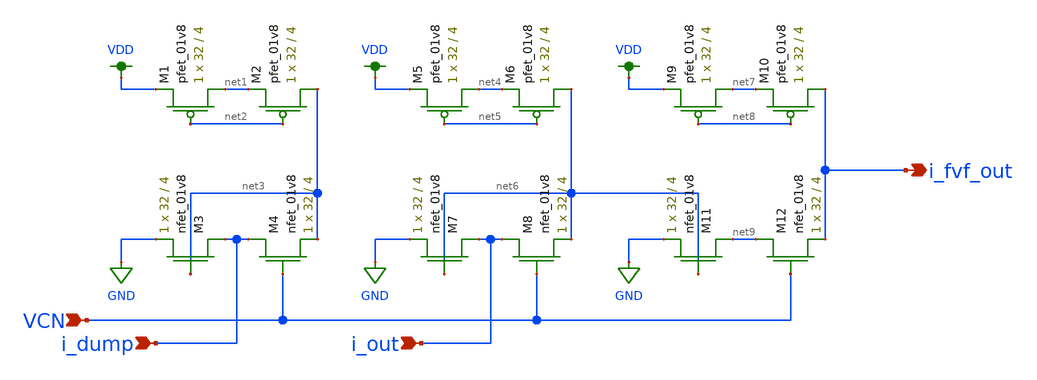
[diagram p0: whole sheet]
** sch_path: schemas/LDS_FVF_BLOCK.sch
**.subckt LDS_FVF_BLOCK i_fvf_out i_dump i_out VCN
*.opin i_fvf_out
*.ipin i_dump
*.ipin i_out
*.ipin VCN
XM1 net1 net2 VDD VDD sky130_fd_pr__pfet_01v8 L=4 W=32 nf=1 ad='int((nf+1)/2) * W/nf * 0.29' as='int((nf+2)/2) * W/nf * 0.29'
+ pd='2*int((nf+1)/2) * (W/nf + 0.29)' ps='2*int((nf+2)/2) * (W/nf + 0.29)' nrd='0.29 / W' nrs='0.29 / W'
+ sa=0 sb=0 sd=0 mult=1 m=1
XM2 net3 net2 net1 VDD sky130_fd_pr__pfet_01v8 L=4 W=32 nf=1 ad='int((nf+1)/2) * W/nf * 0.29' as='int((nf+2)/2) * W/nf * 0.29'
+ pd='2*int((nf+1)/2) * (W/nf + 0.29)' ps='2*int((nf+2)/2) * (W/nf + 0.29)' nrd='0.29 / W' nrs='0.29 / W'
+ sa=0 sb=0 sd=0 mult=1 m=1
XM3 i_dump net3 GND GND sky130_fd_pr__nfet_01v8 L=4 W=32 nf=1 ad='int((nf+1)/2) * W/nf * 0.29' as='int((nf+2)/2) * W/nf * 0.29'
+ pd='2*int((nf+1)/2) * (W/nf + 0.29)' ps='2*int((nf+2)/2) * (W/nf + 0.29)' nrd='0.29 / W' nrs='0.29 / W'
+ sa=0 sb=0 sd=0 mult=1 m=1
XM4 i_dump VCN net3 GND sky130_fd_pr__nfet_01v8 L=4 W=32 nf=1 ad='int((nf+1)/2) * W/nf * 0.29' as='int((nf+2)/2) * W/nf * 0.29'
+ pd='2*int((nf+1)/2) * (W/nf + 0.29)' ps='2*int((nf+2)/2) * (W/nf + 0.29)' nrd='0.29 / W' nrs='0.29 / W'
+ sa=0 sb=0 sd=0 mult=1 m=1
XM5 net4 net5 VDD VDD sky130_fd_pr__pfet_01v8 L=4 W=32 nf=1 ad='int((nf+1)/2) * W/nf * 0.29' as='int((nf+2)/2) * W/nf * 0.29'
+ pd='2*int((nf+1)/2) * (W/nf + 0.29)' ps='2*int((nf+2)/2) * (W/nf + 0.29)' nrd='0.29 / W' nrs='0.29 / W'
+ sa=0 sb=0 sd=0 mult=1 m=1
XM6 net6 net5 net4 VDD sky130_fd_pr__pfet_01v8 L=4 W=32 nf=1 ad='int((nf+1)/2) * W/nf * 0.29' as='int((nf+2)/2) * W/nf * 0.29'
+ pd='2*int((nf+1)/2) * (W/nf + 0.29)' ps='2*int((nf+2)/2) * (W/nf + 0.29)' nrd='0.29 / W' nrs='0.29 / W'
+ sa=0 sb=0 sd=0 mult=1 m=1
XM7 i_out net6 GND GND sky130_fd_pr__nfet_01v8 L=4 W=32 nf=1 ad='int((nf+1)/2) * W/nf * 0.29' as='int((nf+2)/2) * W/nf * 0.29'
+ pd='2*int((nf+1)/2) * (W/nf + 0.29)' ps='2*int((nf+2)/2) * (W/nf + 0.29)' nrd='0.29 / W' nrs='0.29 / W'
+ sa=0 sb=0 sd=0 mult=1 m=1
XM8 i_out VCN net6 GND sky130_fd_pr__nfet_01v8 L=4 W=32 nf=1 ad='int((nf+1)/2) * W/nf * 0.29' as='int((nf+2)/2) * W/nf * 0.29'
+ pd='2*int((nf+1)/2) * (W/nf + 0.29)' ps='2*int((nf+2)/2) * (W/nf + 0.29)' nrd='0.29 / W' nrs='0.29 / W'
+ sa=0 sb=0 sd=0 mult=1 m=1
XM9 net7 net8 VDD VDD sky130_fd_pr__pfet_01v8 L=4 W=32 nf=1 ad='int((nf+1)/2) * W/nf * 0.29' as='int((nf+2)/2) * W/nf * 0.29'
+ pd='2*int((nf+1)/2) * (W/nf + 0.29)' ps='2*int((nf+2)/2) * (W/nf + 0.29)' nrd='0.29 / W' nrs='0.29 / W'
+ sa=0 sb=0 sd=0 mult=1 m=1
XM10 i_fvf_out net8 net7 VDD sky130_fd_pr__pfet_01v8 L=4 W=32 nf=1 ad='int((nf+1)/2) * W/nf * 0.29' as='int((nf+2)/2) * W/nf * 0.29'
+ pd='2*int((nf+1)/2) * (W/nf + 0.29)' ps='2*int((nf+2)/2) * (W/nf + 0.29)' nrd='0.29 / W' nrs='0.29 / W'
+ sa=0 sb=0 sd=0 mult=1 m=1
XM11 net9 net6 GND GND sky130_fd_pr__nfet_01v8 L=4 W=32 nf=1 ad='int((nf+1)/2) * W/nf * 0.29' as='int((nf+2)/2) * W/nf * 0.29'
+ pd='2*int((nf+1)/2) * (W/nf + 0.29)' ps='2*int((nf+2)/2) * (W/nf + 0.29)' nrd='0.29 / W' nrs='0.29 / W'
+ sa=0 sb=0 sd=0 mult=1 m=1
XM12 net9 VCN i_fvf_out GND sky130_fd_pr__nfet_01v8 L=4 W=32 nf=1 ad='int((nf+1)/2) * W/nf * 0.29' as='int((nf+2)/2) * W/nf * 0.29'
+ pd='2*int((nf+1)/2) * (W/nf + 0.29)' ps='2*int((nf+2)/2) * (W/nf + 0.29)' nrd='0.29 / W' nrs='0.29 / W'
+ sa=0 sb=0 sd=0 mult=1 m=1
**.ends
.GLOBAL GND
.GLOBAL VDD
.end
